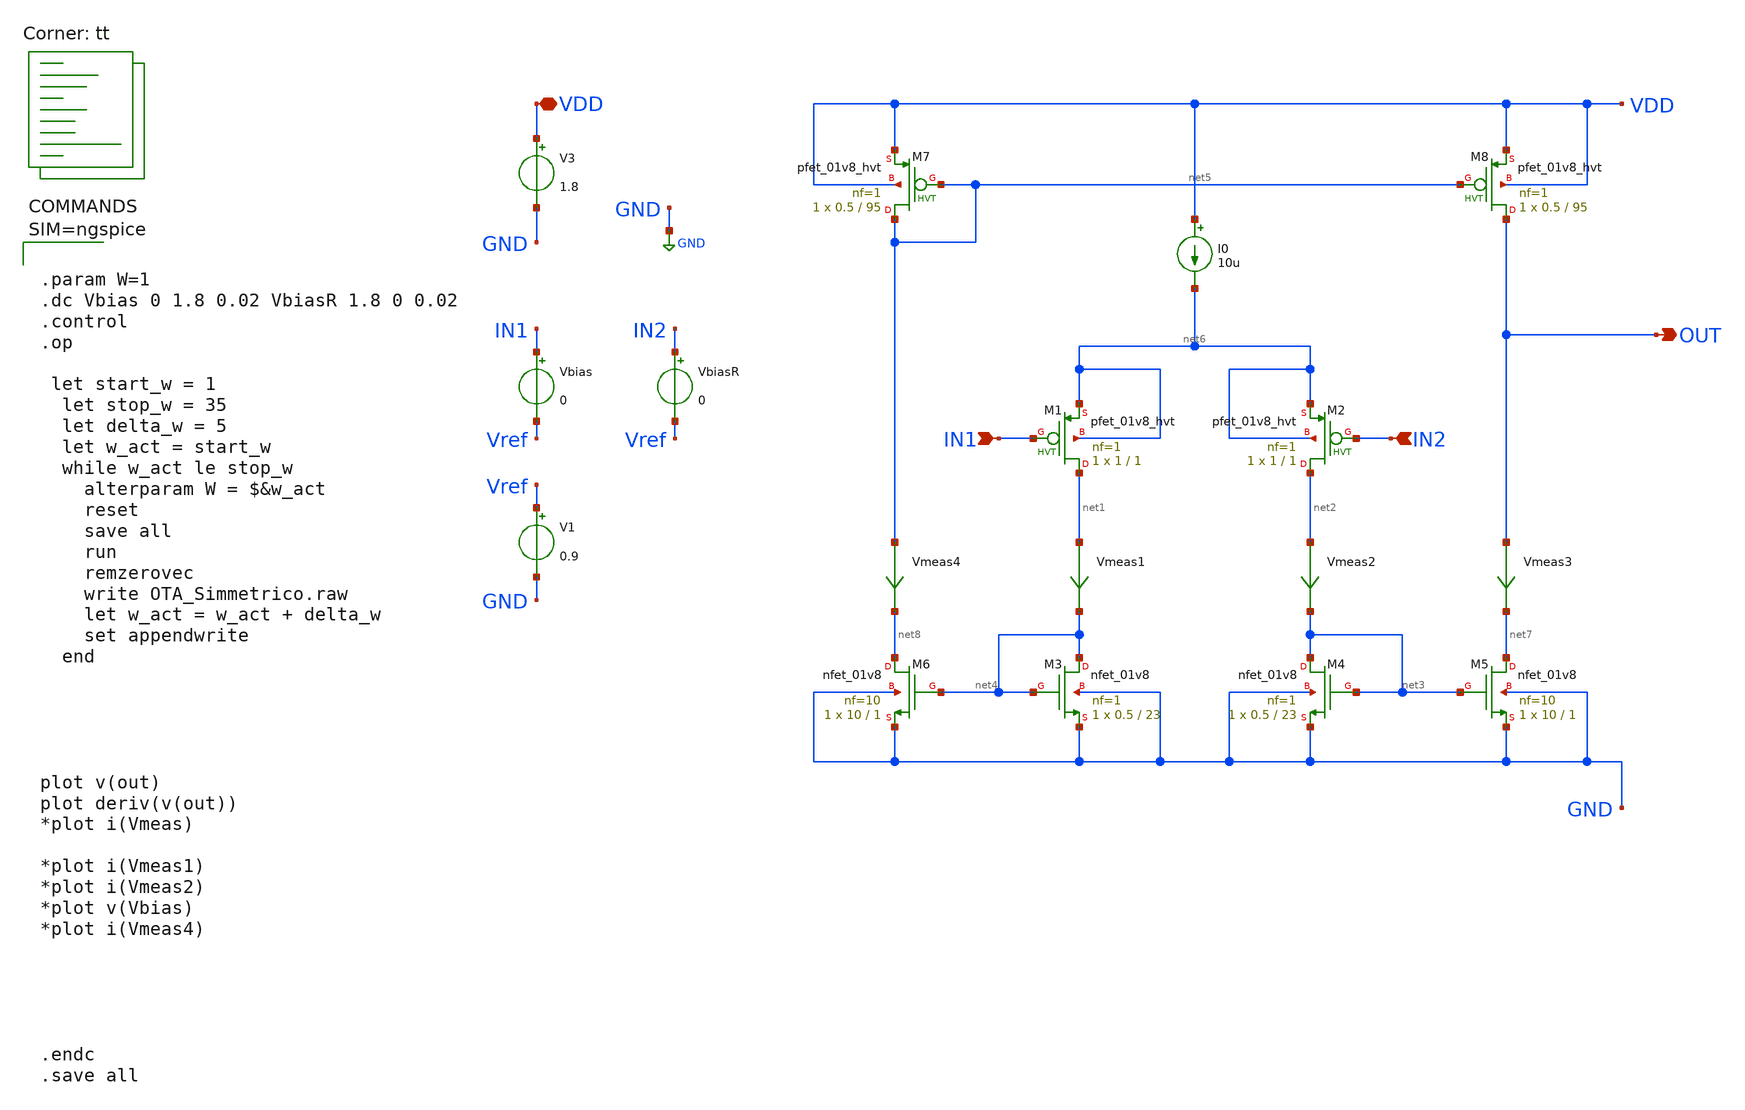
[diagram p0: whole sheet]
** sch_path: xschem/OTA_Simmetrico.sch
**.subckt OTA_Simmetrico VDD IN1 IN2 OUT
*.iopin VDD
*.ipin IN1
*.ipin IN2
*.opin OUT
XM1 net1 IN1 net6 net6 sky130_fd_pr__pfet_01v8_hvt L=1 W=1 nf=1 ad='int((nf+1)/2) * W/nf * 0.29' as='int((nf+2)/2) * W/nf * 0.29'
+ pd='2*int((nf+1)/2) * (W/nf + 0.29)' ps='2*int((nf+2)/2) * (W/nf + 0.29)' nrd='0.29 / W' nrs='0.29 / W'
+ sa=0 sb=0 sd=0 mult=1 m=1
XM2 net2 IN2 net6 net6 sky130_fd_pr__pfet_01v8_hvt L=1 W=1 nf=1 ad='int((nf+1)/2) * W/nf * 0.29' as='int((nf+2)/2) * W/nf * 0.29'
+ pd='2*int((nf+1)/2) * (W/nf + 0.29)' ps='2*int((nf+2)/2) * (W/nf + 0.29)' nrd='0.29 / W' nrs='0.29 / W'
+ sa=0 sb=0 sd=0 mult=1 m=1
XM3 net4 net4 GND GND sky130_fd_pr__nfet_01v8 L=23 W=0.5 nf=1 ad='int((nf+1)/2) * W/nf * 0.29' as='int((nf+2)/2) * W/nf * 0.29'
+ pd='2*int((nf+1)/2) * (W/nf + 0.29)' ps='2*int((nf+2)/2) * (W/nf + 0.29)' nrd='0.29 / W' nrs='0.29 / W'
+ sa=0 sb=0 sd=0 mult=1 m=1
XM4 net3 net3 GND GND sky130_fd_pr__nfet_01v8 L=23 W=0.5 nf=1 ad='int((nf+1)/2) * W/nf * 0.29' as='int((nf+2)/2) * W/nf * 0.29'
+ pd='2*int((nf+1)/2) * (W/nf + 0.29)' ps='2*int((nf+2)/2) * (W/nf + 0.29)' nrd='0.29 / W' nrs='0.29 / W'
+ sa=0 sb=0 sd=0 mult=1 m=1
XM5 net7 net3 GND GND sky130_fd_pr__nfet_01v8 L=1 W=10 nf=10 ad='int((nf+1)/2) * W/nf * 0.29' as='int((nf+2)/2) * W/nf * 0.29'
+ pd='2*int((nf+1)/2) * (W/nf + 0.29)' ps='2*int((nf+2)/2) * (W/nf + 0.29)' nrd='0.29 / W' nrs='0.29 / W'
+ sa=0 sb=0 sd=0 mult=1 m=1
XM6 net8 net4 GND GND sky130_fd_pr__nfet_01v8 L=1 W=10 nf=10 ad='int((nf+1)/2) * W/nf * 0.29' as='int((nf+2)/2) * W/nf * 0.29'
+ pd='2*int((nf+1)/2) * (W/nf + 0.29)' ps='2*int((nf+2)/2) * (W/nf + 0.29)' nrd='0.29 / W' nrs='0.29 / W'
+ sa=0 sb=0 sd=0 mult=1 m=1
XM7 net5 net5 VDD VDD sky130_fd_pr__pfet_01v8_hvt L=95 W=0.5 nf=1 ad='int((nf+1)/2) * W/nf * 0.29' as='int((nf+2)/2) * W/nf * 0.29'
+ pd='2*int((nf+1)/2) * (W/nf + 0.29)' ps='2*int((nf+2)/2) * (W/nf + 0.29)' nrd='0.29 / W' nrs='0.29 / W'
+ sa=0 sb=0 sd=0 mult=1 m=1
XM8 OUT net5 VDD VDD sky130_fd_pr__pfet_01v8_hvt L=95 W=0.5 nf=1 ad='int((nf+1)/2) * W/nf * 0.29' as='int((nf+2)/2) * W/nf * 0.29'
+ pd='2*int((nf+1)/2) * (W/nf + 0.29)' ps='2*int((nf+2)/2) * (W/nf + 0.29)' nrd='0.29 / W' nrs='0.29 / W'
+ sa=0 sb=0 sd=0 mult=1 m=1
Vmeas1 net1 net4 0
.save i(vmeas1)
Vmeas2 net2 net3 0
.save i(vmeas2)
Vmeas3 OUT net7 0
.save i(vmeas3)
Vmeas4 net5 net8 0
.save i(vmeas4)
V3 VDD GND 1.8
Vbias IN1 Vref 0
VbiasR IN2 Vref 0
V1 Vref GND 0.9
I0 VDD net6 10u
**** begin user architecture code
.lib $::SKYWATER_MODELS/sky130.lib.spice tt



.param W=1
.dc Vbias 0 1.8 0.02 VbiasR 1.8 0 0.02
.control
.op

 let start_w = 1
  let stop_w = 35
  let delta_w = 5
  let w_act = start_w
  while w_act le stop_w
    alterparam W = $&w_act
    reset
    save all
    run
    remzerovec
    write OTA_Simmetrico.raw
    let w_act = w_act + delta_w
    set appendwrite
  end





plot v(out)
plot deriv(v(out))
*plot i(Vmeas)

*plot i(Vmeas1)
*plot i(Vmeas2)
*plot v(Vbias)
*plot i(Vmeas4)





.endc
.save all




**** end user architecture code
**.ends
.GLOBAL GND
.end
